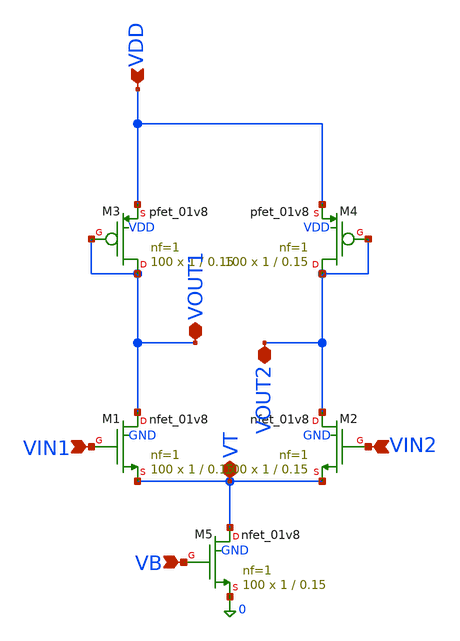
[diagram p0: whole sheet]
** sch_path: MOS-Circuits/Differential Pair/Diff_pair_2/diff_pair_load2.sch
**.subckt diff_pair_load2 VIN1 VIN2 VDD VOUT1 VOUT2 VB VT
*.ipin VIN1
*.ipin VIN2
*.ipin VDD
*.iopin VOUT1
*.iopin VOUT2
*.ipin VB
*.iopin VT
XM1 VOUT1 VIN1 VT GND sky130_fd_pr__nfet_01v8 L=0.15 W=1 nf=1 ad='int((nf+1)/2) * W/nf * 0.29' as='int((nf+2)/2) * W/nf * 0.29'
+ pd='2*int((nf+1)/2) * (W/nf + 0.29)' ps='2*int((nf+2)/2) * (W/nf + 0.29)' nrd='0.29 / W' nrs='0.29 / W'
+ sa=0 sb=0 sd=0 mult=100 m=100
XM2 VOUT2 VIN2 VT GND sky130_fd_pr__nfet_01v8 L=0.15 W=1 nf=1 ad='int((nf+1)/2) * W/nf * 0.29' as='int((nf+2)/2) * W/nf * 0.29'
+ pd='2*int((nf+1)/2) * (W/nf + 0.29)' ps='2*int((nf+2)/2) * (W/nf + 0.29)' nrd='0.29 / W' nrs='0.29 / W'
+ sa=0 sb=0 sd=0 mult=100 m=100
XM3 VOUT1 VOUT1 VDD VDD sky130_fd_pr__pfet_01v8 L=0.15 W=1 nf=1 ad='int((nf+1)/2) * W/nf * 0.29' as='int((nf+2)/2) * W/nf * 0.29'
+ pd='2*int((nf+1)/2) * (W/nf + 0.29)' ps='2*int((nf+2)/2) * (W/nf + 0.29)' nrd='0.29 / W' nrs='0.29 / W'
+ sa=0 sb=0 sd=0 mult=100 m=100
XM4 VOUT2 VOUT2 VDD VDD sky130_fd_pr__pfet_01v8 L=0.15 W=1 nf=1 ad='int((nf+1)/2) * W/nf * 0.29' as='int((nf+2)/2) * W/nf * 0.29'
+ pd='2*int((nf+1)/2) * (W/nf + 0.29)' ps='2*int((nf+2)/2) * (W/nf + 0.29)' nrd='0.29 / W' nrs='0.29 / W'
+ sa=0 sb=0 sd=0 mult=100 m=100
XM5 VT VB 0 GND sky130_fd_pr__nfet_01v8 L=0.15 W=1 nf=1 ad='int((nf+1)/2) * W/nf * 0.29' as='int((nf+2)/2) * W/nf * 0.29'
+ pd='2*int((nf+1)/2) * (W/nf + 0.29)' ps='2*int((nf+2)/2) * (W/nf + 0.29)' nrd='0.29 / W' nrs='0.29 / W'
+ sa=0 sb=0 sd=0 mult=100 m=100
**.ends
.end
